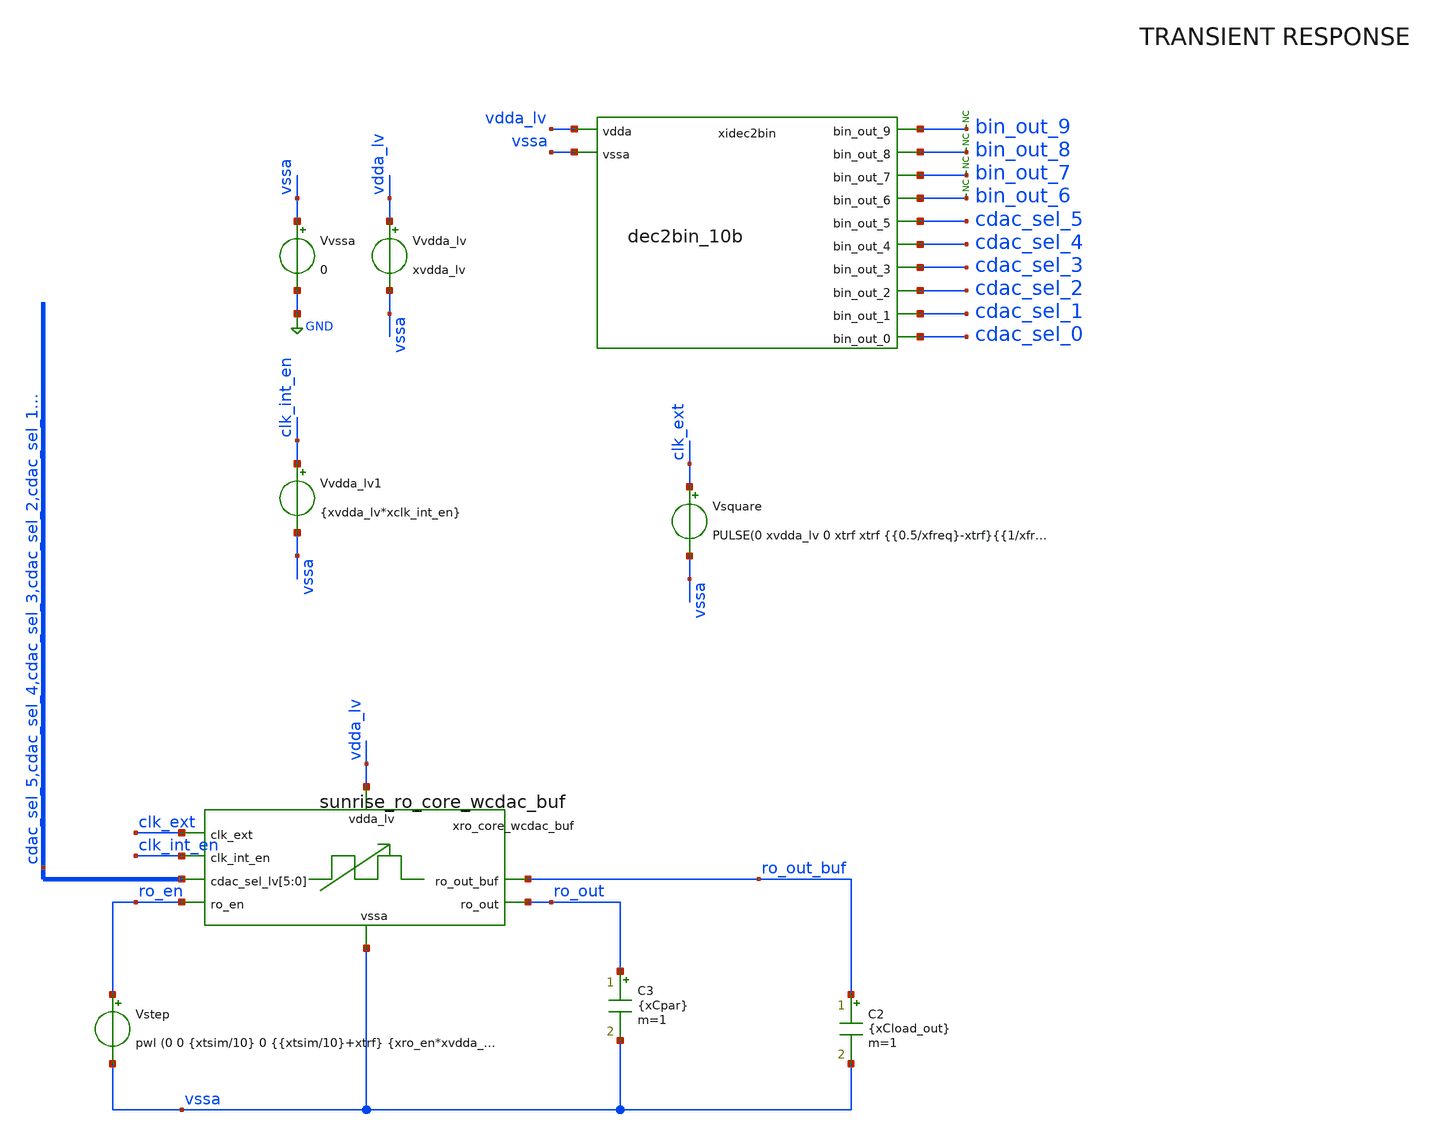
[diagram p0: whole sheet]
** sch_path: Design_Review_2/RO/Testbench1_tb_sunrise_ringosc/tb_sunrise_ringosc.sch
**.subckt tb_sunrise_ringosc
Vvssa vssa GND 0
Vvdda_lv vdda_lv vssa xvdda_lv
Vstep ro_en vssa pwl (0 0 {xtsim/10} 0 {{xtsim/10}+xtrf} {xro_en*xvdda_lv})
C2 ro_out_buf vssa {xCload_out} m=1
xidec2bin bin_out_9 bin_out_8 bin_out_7 bin_out_6 cdac_sel_5 cdac_sel_4 cdac_sel_3 cdac_sel_2
+ cdac_sel_1 cdac_sel_0 vdda_lv vssa dec2bin_10b dec_code=dec_code_var
* noconn bin_out_9
* noconn bin_out_8
* noconn bin_out_7
* noconn bin_out_6
C3 ro_out vssa {xCpar} m=1
xro_core_wcdac_buf vdda_lv ro_out_buf cdac_sel_5 cdac_sel_4 cdac_sel_3 cdac_sel_2 cdac_sel_1
+ cdac_sel_0 ro_en vssa ro_out clk_ext clk_int_en sunrise_ro_core_wcdac_buf
Vvdda_lv1 clk_int_en vssa {xvdda_lv*xclk_int_en}
Vsquare clk_ext vssa PULSE(0 xvdda_lv 0 xtrf xtrf {{0.5/xfreq}-xtrf}{{1/xfreq}-xtrf})
**** begin user architecture code

** opencircuitdesign pdks install

.lib /home/slice/pdk/iHP/IHP-Open-PDK/ihp-sg13g2/libs.tech/ngspice/models/cornerMOShv.lib mos_tt
* SG13G2 STD CELLS
*.include /home/slice/pdk/iHP/IHP-Open-PDK/ihp-sg13g2/libs.ref/sg13g2_stdcell/spice/sg13g2_stdcell.spice
* SG13CMOS5L STD CELLS
.include /home/slice/pdk/iHP/IHP-Open-PDK/ihp-sg13cmos5l/libs.ref/sg13cmos5l_stdcell/spice/sg13cmos5l_stdcell.spice
*ftyp
.lib /home/slice/pdk/iHP/IHP-Open-PDK/ihp-sg13g2/libs.tech/ngspice/models/cornerMOSlv.lib mos_tt
.lib /home/slice/pdk/iHP/IHP-Open-PDK/ihp-sg13g2/libs.tech/ngspice/models/cornerRES.lib res_typ
*fmax
*.lib /home/slice/pdk/iHP/IHP-Open-PDK/ihp-sg13g2/libs.tech/ngspice/models/cornerMOSlv.lib mos_ss
*.lib /home/slice/pdk/iHP/IHP-Open-PDK/ihp-sg13g2/libs.tech/ngspice/models/cornerRES.lib res_bcs
*fmin
*.lib /home/slice/pdk/iHP/IHP-Open-PDK/ihp-sg13g2/libs.tech/ngspice/models/cornerMOSlv.lib mos_ff
*.lib /home/slice/pdk/iHP/IHP-Open-PDK/ihp-sg13g2/libs.tech/ngspice/models/cornerRES.lib res_wcs

* required because I used the filler std cells in error that create 6 floating wells which ngspice
*+ cant converge on.
* should have used decap std cells and was too much effort to change. use decap cells in future.
.option rshunt=1e22


** PARAMETERS **

* global parameters
.param xvdda_lv = 1.425
.csparam xvdda_lv_var = 'xvdda_lv'
.param xvdda_hv = 3.3
.csparam xvdda_hv_var = 'xvdda_hv'
.param cor_id = 0
.csparam cor_id_var = 'cor_id'
.param xtsim = 1.2u
.csparam xtsim_var = 'xtsim'
.param xtstep = 1n
.csparam xtstep_var = 'xtstep'
.param dec_code_var = 12
.param xCload = 5p
.param xtrf = 20p
.param xfreq = 10e6
.param xCpar = 0f
.param xclk_int_en = 1
.param xCload_out = 1p
.param xCload_int = 1p
.param xCdac_unit = 300f
.param xCro_unit = 1.2p
.param xRload_int = 10k
.param xtrf = 20p
.param xro_en = 1

.temp 27

* vlogA instantiations
*.model OTA_vcvs OTA_vcvs
*.model ideal_sw ideal_sw
.model dec2bin_10b dec2bin_10b

.include tb_sunrise_ringosc.save

* below line needs to be included if running ac noise analysys
*.save all
.save v(ro_out) v(ro_out_buf) i(vvdda_lv) v(xro_core_wcdac_buf.xro_wcdac.xro_core.n0) v(xro_core_wcdac_buf.xro_wcdac.xro_core.n1) v(xro_core_wcdac_buf.xro_wcdac.xro_core.n2) v(xro_core_wcdac_buf.xro_wcdac.xro_core.n3) v(xro_core_wcdac_buf.xro_wcdac.xro_core.n4) v(xro_core_wcdac_buf.xro_wcdac.xro_core.n5) v(xro_core_wcdac_buf.xro_wcdac.xro_core.n6) v(xro_core_wcdac_buf.xro_wcdac.xro_core.n7) v(xro_core_wcdac_buf.xro_wcdac.xro_core.n8) v(xro_core_wcdac_buf.xro_wcdac.xro_core.n9) v(xro_core_wcdac_buf.xro_wcdac.xro_core.n10) v(clk_ext)

*.option savecurrents

.control

  let xdec_code_var = 31

   repeat  1              ; loop start
   alterparam dec_code_var = $&xdec_code_var;        ; alter the decimal code
   reset

*pre_osdi OTA_vcvs.osdi
*pre_osdi ideal_sw.osdi
pre_osdi dec2bin_10b.osdi

 * commercial temperature range
 *set xTj = ( 0 10 20 30 40 50 60 70 )
 * industrial temperature range
 *set xTj = ( -40 -30 -20 -10 0 10 20 30 40 50 60 70 85 )
 * military temperature range
 *set xTj = ( -55 -40 -30 -20 -10 0 10 20 30 40 50 60 70 80 90 100 110 125 )
 *set xTj = ( -55 -50 -45 -40 -35 -30 -25 -20 -15 -10 -5 0 5 10 15 20 25 30 35 40 45 50 55 60 65 70
+ 75 80 85 90 95 100 105 110 115 120 125 )
 * automotive temperature range
 *set xTj = ( -40 -30 -20 -10 0 10 20 30 40 50 60 70 80 90 100 110 120 130 140 150 )
 set xTj = ( 27 )

  foreach xTj_var $xTj

  let Tj_meas = $xTj_var

  echo temperature is "$&Tj_meas"

  *echo "$&Tj_meas" >> Temp_measures.txt

  set temp = $xTj_var
  echo $temp

** 0. DCOP ANALYSIS **

  op
  remzerovec
  set filetype=binary
  ** first write deletes existing file
  write tb_sunrise_ro_dcop.raw

** 1. TRAN ANALYSIS **

  *remzerovec *** always put remzerovec after the analysis!!!
  *set appendwrite
  tran $&xtstep_var $&xtsim_var
  remzerovec
  write tb_sunrise_ro_tran.raw
 *unset appendwrite
 option

** 2. TRAN MEASURES **

  echo --
  meas tran idda_ave AVG i(vvdda_lv) from=1n to=$&xtsim_var
  let idda_ave_uA = idda_ave*(-1e6)
  meas tran ro_out_max MAX v(ro_out) from=1n to=$&xtsim_var
  meas tran ro_out_min MIN v(ro_out) from=1n to=$&xtsim_var
  let ro_out_p2p = ro_out_max - ro_out_min
  meas tran Tro23 TRIG v(ro_out_buf) VAL=0.5*$&xvdda_lv_var FALL=2 TARG v(ro_out_buf)
+ VAL=0.5*$&xvdda_lv_var FALL=3
    meas tran Tro45 TRIG v(ro_out_buf) VAL=0.5*$&xvdda_lv_var FALL=4 TARG v(ro_out_buf)
+ VAL=0.5*$&xvdda_lv_var FALL=5
      meas tran Tro67 TRIG v(ro_out_buf) VAL=0.5*$&xvdda_lv_var FALL=6 TARG v(ro_out_buf)
+ VAL=0.5*$&xvdda_lv_var FALL=7
        meas tran Tro89 TRIG v(ro_out_buf) VAL=0.5*$&xvdda_lv_var FALL=8 TARG v(ro_out_buf)
+ VAL=0.5*$&xvdda_lv_var FALL=9
  let Tro = (Tro23+Tro45+Tro67+Tro89)/4
  let freq_ro_MHz=(1/Tro)*1e-6
  meas tran pw TRIG v(ro_out_buf) VAL=0.5*$&xvdda_lv_var RISE=3 TARG v(ro_out_buf)
+ VAL=0.5*$&xvdda_lv_var FALL=4
  * below measures pw for an external clk
  *meas tran pw TRIG v(ro_out_buf) VAL=0.5*$&xvdda_lv_var RISE=3 TARG v(ro_out_buf)
+ VAL=0.5*$&xvdda_lv_var FALL=3
  let D_cyc_per=(pw/Tro)*100
  meas tran n0_max MAX v(xro_core_wcdac_buf.xro_wcdac.xro_core.n0) from=1n to=$&xtsim_var
  meas tran n0_min MIN v(xro_core_wcdac_buf.xro_wcdac.xro_core.n0) from=1n to=$&xtsim_var
  let n0_p2p = n0_max - n0_min
  meas tran n1_max MAX v(xro_core_wcdac_buf.xro_wcdac.xro_core.n1) from=1n to=$&xtsim_var
  meas tran n1_min MIN v(xro_core_wcdac_buf.xro_wcdac.xro_core.n1) from=1n to=$&xtsim_var
  let n1_p2p = n1_max - n1_min
  meas tran n2_max MAX v(xro_core_wcdac_buf.xro_wcdac.xro_core.n2) from=1n to=$&xtsim_var
  meas tran n2_min MIN v(xro_core_wcdac_buf.xro_wcdac.xro_core.n2) from=1n to=$&xtsim_var
  let n2_p2p = n2_max - n2_min
  meas tran n3_max MAX v(xro_core_wcdac_buf.xro_wcdac.xro_core.n3) from=1n to=$&xtsim_var
  meas tran n3_min MIN v(xro_core_wcdac_buf.xro_wcdac.xro_core.n3) from=1n to=$&xtsim_var
  let n3_p2p = n3_max - n3_min
  meas tran n4_max MAX v(xro_core_wcdac_buf.xro_wcdac.xro_core.n4) from=1n to=$&xtsim_var
  meas tran n4_min MIN v(xro_core_wcdac_buf.xro_wcdac.xro_core.n4) from=1n to=$&xtsim_var
  let n4_p2p = n4_max - n4_min
  meas tran n5_max MAX v(xro_core_wcdac_buf.xro_wcdac.xro_core.n5) from=1n to=$&xtsim_var
  meas tran n5_min MIN v(xro_core_wcdac_buf.xro_wcdac.xro_core.n5) from=1n to=$&xtsim_var
  let n5_p2p = n5_max - n5_min
  meas tran n6_max MAX v(xro_core_wcdac_buf.xro_wcdac.xro_core.n6) from=1n to=$&xtsim_var
  meas tran n6_min MIN v(xro_core_wcdac_buf.xro_wcdac.xro_core.n6) from=1n to=$&xtsim_var
  let n6_p2p = n6_max - n6_min
  meas tran n7_max MAX v(xro_core_wcdac_buf.xro_wcdac.xro_core.n7) from=1n to=$&xtsim_var
  meas tran n7_min MIN v(xro_core_wcdac_buf.xro_wcdac.xro_core.n7) from=1n to=$&xtsim_var
  let n7_p2p = n7_max - n7_min
  meas tran n8_max MAX v(xro_core_wcdac_buf.xro_wcdac.xro_core.n8) from=1n to=$&xtsim_var
  meas tran n8_min MIN v(xro_core_wcdac_buf.xro_wcdac.xro_core.n8) from=1n to=$&xtsim_var
  let n8_p2p = n8_max - n8_min
  meas tran n9_max MAX v(xro_core_wcdac_buf.xro_wcdac.xro_core.n9) from=1n to=$&xtsim_var
  meas tran n9_min MIN v(xro_core_wcdac_buf.xro_wcdac.xro_core.n9) from=1n to=$&xtsim_var
  let n9_p2p = n9_max - n9_min
  meas tran n10_max MAX v(xro_core_wcdac_buf.xro_wcdac.xro_core.n10) from=1n to=$&xtsim_var
  meas tran n10_min MIN v(xro_core_wcdac_buf.xro_wcdac.xro_core.n10) from=1n to=$&xtsim_var
  let n10_p2p = n10_max - n10_min

  * 3.0 Global parameters:
  *echo cor_id = "$&cor_id_var"
  *echo "$&cor_id_var" >> idda_uA.txt
  *echo "$&cor_id_var" >> freq_ro_MHz.txt
  *echo "$&cor_id_var" >> Dcyc_per.txt
  *echo "$&cor_id_var" >> ro_max.txt
  *echo "$&cor_id_var" >> ro_min.txt
  *echo "$&cor_id_var" >> ro_p2p.txt
  echo code = "$&xdec_code_var"
  *echo "$&xdec_code_var" >> idda_uA.txt
  *echo "$&xdec_code_var" >> freq_ro_MHz.txt
  *echo "$&xdec_code_var" >> Dcyc_per.txt
  *echo "$&xdec_code_var" >> ro_max.txt
  *echo "$&xdec_code_var" >> ro_min.txt
  *echo "$&xdec_code_var" >> ro_p2p.txt
  echo --
  echo temp = "$temp"
  *echo "$temp" >> idda_uA.txt
  *echo "$temp" >> freq_ro_MHz.txt
  *echo "$temp" >> Dcyc_per.txt
  *echo "$temp" >> ro_max.txt
  *echo "$temp" >> ro_min.txt
  *echo "$temp" >> ro_p2p.txt
  echo --
  echo vdda_hv = "$&xvdda_hv_var"
  *echo "$&xvdda_hv_var" >> idda_uA.txt
  *echo "$&xvdda_hv_var" >> freq_ro_MHz.txt
  *echo "$&xvdda_hv_var" >> Dcyc_per.txt
  *echo "$&xvdda_hv_var" >> ro_max.txt
  *echo "$&xvdda_hv_var" >> ro_min.txt
  *echo "$&xvdda_hv_var" >> ro_p2p.txt
  echo --
  echo vdda_lv = "$&xvdda_lv_var"
  *echo "$&xvdda_lv_var" >> idda_uA.txt
  *echo "$&xvdda_lv_var" >> freq_ro_MHz.txt
  *echo "$&xvdda_lv_var" >> ro_max.txt
  *echo "$&xvdda_lv_var" >> ro_min.txt
  *echo "$&xvdda_lv_var" >> ro_p2p.txt
  echo --
  echo temp = "$temp"
  echo "$temp" >> Temperature.txt
  echo  idda_uA = "$&idda_ave_uA"
  echo "$&idda_ave_uA" >> idda_uA.txt
  echo  freq_MHz = "$&freq_ro_MHz"
  echo "$&freq_ro_MHz" >> freq_ro_MHz.txt
  echo  D_cyc = "$&D_cyc_per"
  echo "$&D_cyc_per" >> Dcyc_per.txt
  echo  ro_out_max = "$&ro_out_max"
  echo "$&ro_out_max" >> ro_max.txt
  echo  ro_out_min = "$&ro_out_min"
  echo "$&ro_out_min" >> ro_min.txt
  echo  ro_out_p2p = "$&ro_out_p2p"
  echo "$&ro_out_p2p" >> ro_p2p.txt
  echo  n0_p2p = "$&n0_p2p"
  echo "$&n0_p2p" >> n0_p2p.txt
  echo  n1_p2p = "$&n1_p2p"
  echo "$&n1_p2p" >> n1_p2p.txt
  echo  n2_p2p = "$&n2_p2p"
  echo "$&n2_p2p" >> n2_p2p.txt
  echo  n3_p2p = "$&n3_p2p"
  echo "$&n3_p2p" >> n3_p2p.txt
  echo  n4_p2p = "$&n4_p2p"
  echo "$&n4_p2p" >> n4_p2p.txt
  echo  n5_p2p = "$&n5_p2p"
  echo "$&n5_p2p" >> n5_p2p.txt
  echo  n6_p2p = "$&n6_p2p"
  echo "$&n6_p2p" >> n6_p2p.txt
  echo  n7_p2p = "$&n7_p2p"
  echo "$&n7_p2p" >> n7_p2p.txt
  echo  n8_p2p = "$&n8_p2p"
  echo "$&n8_p2p" >> n8_p2p.txt
  echo  n9_p2p = "$&n9_p2p"
  echo "$&n9_p2p" >> n9_p2p.txt
  echo  n10_p2p = "$&n10_p2p"
  echo "$&n10_p2p" >> n10_p2p.txt
  echo --

   let xdec_code_var = xdec_code_var + 1;
   end

  end

  setplot
*quit 0
.endc




**** end user architecture code
**.ends
.GLOBAL GND
.end
